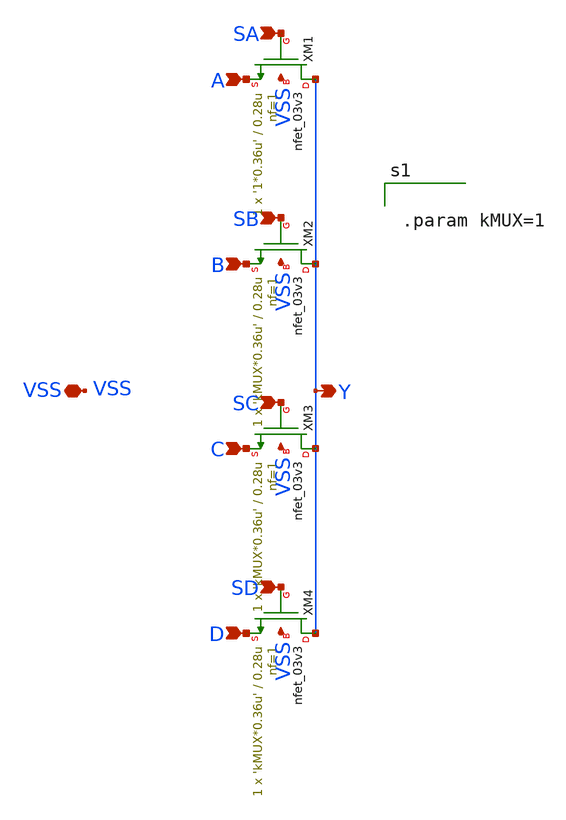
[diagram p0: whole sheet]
** sch_path: CAD4/4x1_mux.sch
**.subckt 4x1_mux A B C D Y VSS SA SB SC SD
*.ipin A
*.ipin B
*.ipin C
*.ipin D
*.opin Y
*.iopin VSS
*.ipin SA
*.ipin SB
*.ipin SC
*.ipin SD
XM1 Y SA A VSS nfet_03v3 L=0.28u W='1*0.36u' nf=1 ad='int((nf+1)/2) * W/nf * 0.18u' as='int((nf+2)/2) * W/nf * 0.18u'
+ pd='2*int((nf+1)/2) * (W/nf + 0.18u)' ps='2*int((nf+2)/2) * (W/nf + 0.18u)' nrd='0.18u / W' nrs='0.18u / W'
+ sa=0 sb=0 sd=0 m=1
XM2 Y SB B VSS nfet_03v3 L=0.28u W='kMUX*0.36u' nf=1 ad='int((nf+1)/2) * W/nf * 0.18u' as='int((nf+2)/2) * W/nf * 0.18u'
+ pd='2*int((nf+1)/2) * (W/nf + 0.18u)' ps='2*int((nf+2)/2) * (W/nf + 0.18u)' nrd='0.18u / W' nrs='0.18u / W'
+ sa=0 sb=0 sd=0 m=1
XM3 Y SC C VSS nfet_03v3 L=0.28u W='kMUX*0.36u' nf=1 ad='int((nf+1)/2) * W/nf * 0.18u' as='int((nf+2)/2) * W/nf * 0.18u'
+ pd='2*int((nf+1)/2) * (W/nf + 0.18u)' ps='2*int((nf+2)/2) * (W/nf + 0.18u)' nrd='0.18u / W' nrs='0.18u / W'
+ sa=0 sb=0 sd=0 m=1
XM4 Y SD D VSS nfet_03v3 L=0.28u W='kMUX*0.36u' nf=1 ad='int((nf+1)/2) * W/nf * 0.18u' as='int((nf+2)/2) * W/nf * 0.18u'
+ pd='2*int((nf+1)/2) * (W/nf + 0.18u)' ps='2*int((nf+2)/2) * (W/nf + 0.18u)' nrd='0.18u / W' nrs='0.18u / W'
+ sa=0 sb=0 sd=0 m=1
**** begin user architecture code


.param kMUX=1


**** end user architecture code
**.ends
.end
